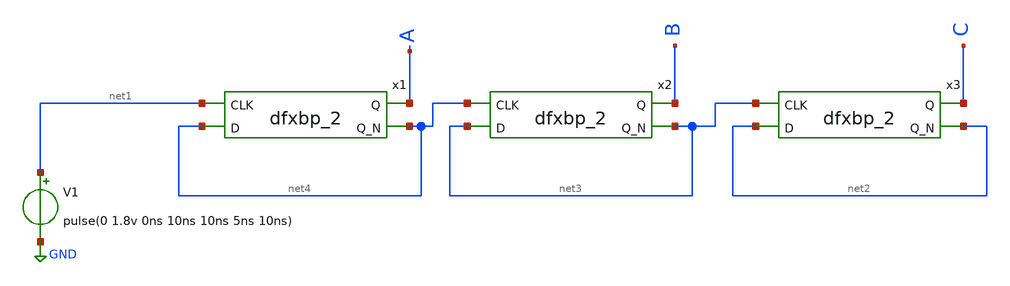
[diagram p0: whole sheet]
** sch_path: xschem/FD.sch
**.subckt FD
x1 net1 net4 VGND VNB VPB VPWR A net4 sky130_fd_sc_hd__dfxbp_2
x2 net4 net3 VGND VNB VPB VPWR B net3 sky130_fd_sc_hd__dfxbp_2
x3 net3 net2 VGND VNB VPB VPWR C net2 sky130_fd_sc_hd__dfxbp_2
V1 net1 GND pulse(0 1.8v 0ns 10ns 10ns 5ns 10ns)
**.ends
.GLOBAL GND
.end
